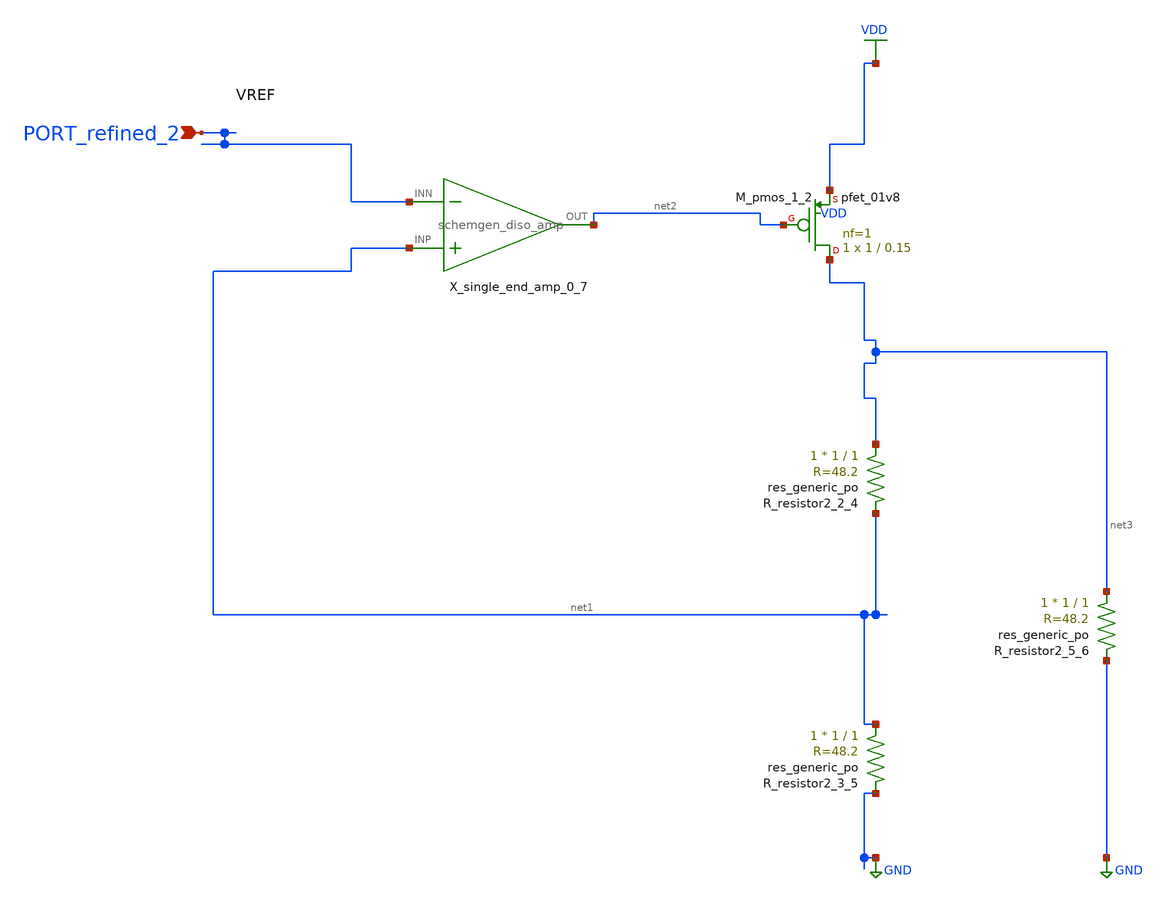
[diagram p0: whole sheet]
** sch_path: schematics/Image2Net/101.sch
**.subckt 101 PORT_refined_2
*.ipin PORT_refined_2
XM_pmos_1_2 net3 net2 VDD VDD sky130_fd_pr__pfet_01v8 L=0.15 W=1 nf=1 ad='int((1 + 1)/2) * 1 / 1 * 0.29'
+ as='int((1 + 2)/2) * 1 / 1 * 0.29' pd='2*int((1 + 1)/2) * (1 / 1 + 0.29)' ps='2*int((1 + 2)/2) * (1 / 1 + 0.29)'
+ nrd='0.29 / 1 ' nrs='0.29 / 1 ' sa=0 sb=0 sd=0 mult=1 m=1
XR_resistor2_2_4 net3 net1 sky130_fd_pr__res_generic_po W=1 L=1 m=1
XR_resistor2_3_5 net1 GND sky130_fd_pr__res_generic_po W=1 L=1 m=1
XR_resistor2_5_6 net3 GND sky130_fd_pr__res_generic_po W=1 L=1 m=1
X_single_end_amp_0_7 net1 PORT_refined_2 net2 schemgen_diso_amp
**.ends

* expanding   symbol:  schemgen_diso_amp.sym # of pins=3
** sym_path: symbols/schemgen_diso_amp.sym
.subckt schemgen_diso_amp INP INN OUT
* SchemGen ideal op-amp: Vout = 1e5 * (V(INP) - V(INN))
E1 OUT 0 INP INN 1e5
.ends schemgen_diso_amp
.GLOBAL GND
.GLOBAL VDD
.end
